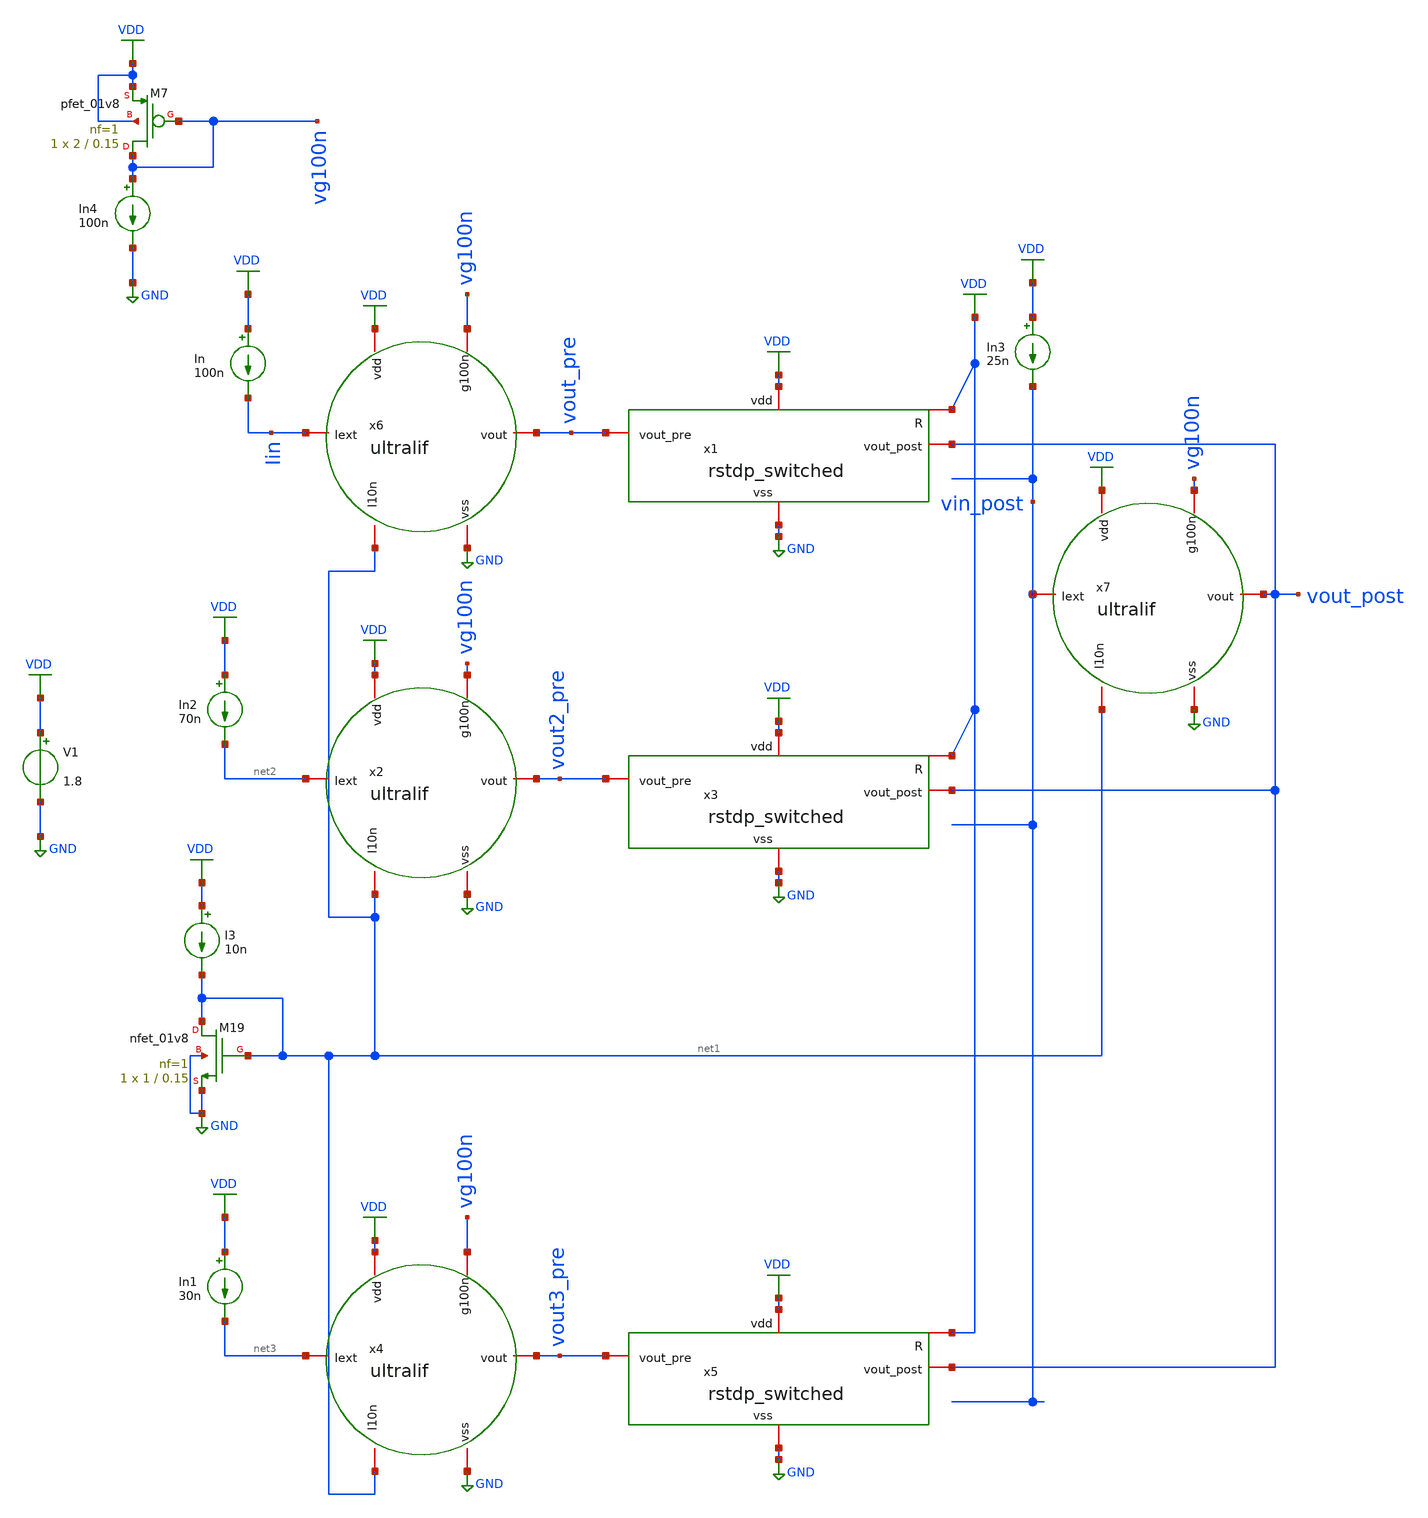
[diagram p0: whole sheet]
** sch_path: tb_1_1.sch
**.subckt tb_1_1
V1 VDD GND 1.8
x6 VDD Iin vout_pre net1 GND vg100n ultralif
x7 VDD vin_post vout_post net1 GND vg100n ultralif
XM19 net1 net1 GND GND sky130_fd_pr__nfet_01v8 L=0.15 W=1 nf=1 ad='int((nf+1)/2) * W/nf * 0.29' as='int((nf+2)/2) * W/nf * 0.29'
+ pd='2*int((nf+1)/2) * (W/nf + 0.29)' ps='2*int((nf+2)/2) * (W/nf + 0.29)' nrd='0.29 / W' nrs='0.29 / W'
+ sa=0 sb=0 sd=0 mult=1 m=1
I3 VDD net1 10n
x1 VDD VDD GND vout_pre vout_post rstdp_switched
In VDD Iin 100n
x2 VDD net2 vout2_pre net1 GND vg100n ultralif
In2 VDD net2 70n
x3 VDD VDD GND vout2_pre vout_post rstdp_switched
x4 VDD net3 vout3_pre net1 GND vg100n ultralif
In1 VDD net3 30n
x5 VDD VDD GND vout3_pre vout_post rstdp_switched
In3 VDD vin_post 25n
XM7 vg100n vg100n VDD VDD sky130_fd_pr__pfet_01v8 L=0.15 W=2 nf=1 ad='int((nf+1)/2) * W/nf * 0.29' as='int((nf+2)/2) * W/nf * 0.29'
+ pd='2*int((nf+1)/2) * (W/nf + 0.29)' ps='2*int((nf+2)/2) * (W/nf + 0.29)' nrd='0.29 / W' nrs='0.29 / W'
+ sa=0 sb=0 sd=0 mult=1 m=1
In4 vg100n GND 100n
**** begin user architecture code
.lib $::SKYWATER_MODELS/sky130.lib.spice tt

** opencircuitdesign pdks install
.inc $::SKYWATER_MODELS/rram_v0.spice

**** end user architecture code
**.ends
.GLOBAL VDD
.GLOBAL GND
**** begin user architecture code


*.options savecurrents
.tran 100n 50u uic
.control
	run
	write tb_1_1.raw
.endc


**** end user architecture code
.end
